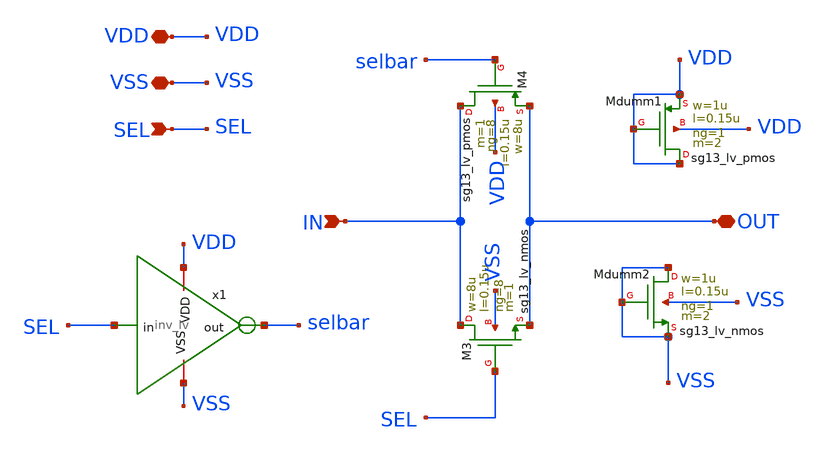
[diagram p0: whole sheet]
** sch_path: xschem/tg_lv.sch
**.subckt tg_lv IN VDD VSS OUT SEL
*.ipin IN
*.iopin VDD
*.iopin VSS
*.iopin OUT
*.ipin SEL
x1 VDD SEL selbar VSS inv_lv
XM3 IN SEL OUT VSS sg13_lv_nmos w=8u l=0.15u ng=8 m=1 mm_ok=1
XM4 IN selbar OUT VDD sg13_lv_pmos w=8u l=0.15u ng=8 m=1 mm_ok=1
XMdumm1 VDD VDD VDD VDD sg13_lv_pmos w=1u l=0.15u ng=1 m=2 mm_ok=1
XMdumm2 VSS VSS VSS VSS sg13_lv_nmos w=1u l=0.15u ng=1 m=2 mm_ok=1
**.ends
.end
